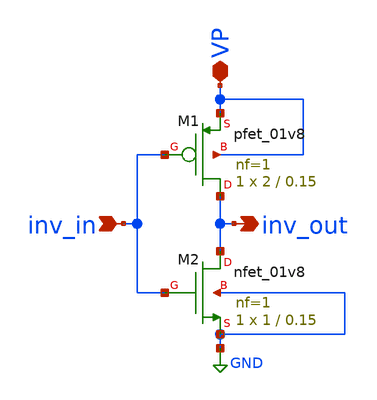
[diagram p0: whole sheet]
** sch_path: AllSymbols&Sch/GenericSym/inverter.sch
**.subckt inverter inv_in inv_out VP
*.ipin inv_in
*.opin inv_out
*.iopin VP
XM1 inv_out inv_in VP VP sky130_fd_pr__pfet_01v8 L=0.15 W=2 nf=1 ad='int((1 + 1)/2) * 2 / 1 * 0.29' as='int((1 + 2)/2) * 2 / 1 * 0.29'
+ pd='2*int((1 + 1)/2) * (2 / 1 + 0.29)' ps='2*int((1 + 2)/2) * (2 / 1 + 0.29)' nrd='0.29 / 2 ' nrs='0.29 / 2 '
+ sa=0 sb=0 sd=0 mult=1 m=1
XM2 inv_out inv_in GND GND sky130_fd_pr__nfet_01v8 L=0.15 W=1 nf=1 ad='int((1 + 1)/2) * 1 / 1 * 0.29'
+ as='int((1 + 2)/2) * 1 / 1 * 0.29' pd='2*int((1 + 1)/2) * (1 / 1 + 0.29)' ps='2*int((1 + 2)/2) * (1 / 1 + 0.29)'
+ nrd='0.29 / 1 ' nrs='0.29 / 1 ' sa=0 sb=0 sd=0 mult=1 m=1
**.ends
.GLOBAL GND
.end
